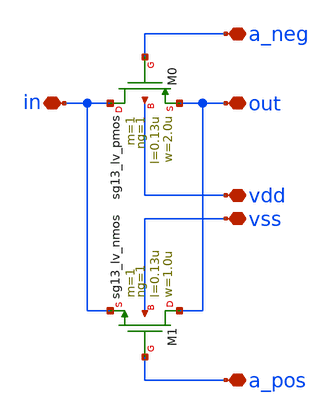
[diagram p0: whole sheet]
** sch_path: design/blocks/transmissiongate/schematic/transmissiongate.sch
**.subckt transmissiongate vdd vss out in a_neg a_pos
*.iopin vdd
*.iopin vss
*.iopin out
*.iopin in
*.iopin a_neg
*.iopin a_pos
XM0 in a_neg out vdd sg13_lv_pmos w=2.0u l=0.13u ng=1 m=1 mm_ok=1
XM1 out a_pos in vss sg13_lv_nmos w=1.0u l=0.13u ng=1 m=1 mm_ok=1
**.ends
.end
